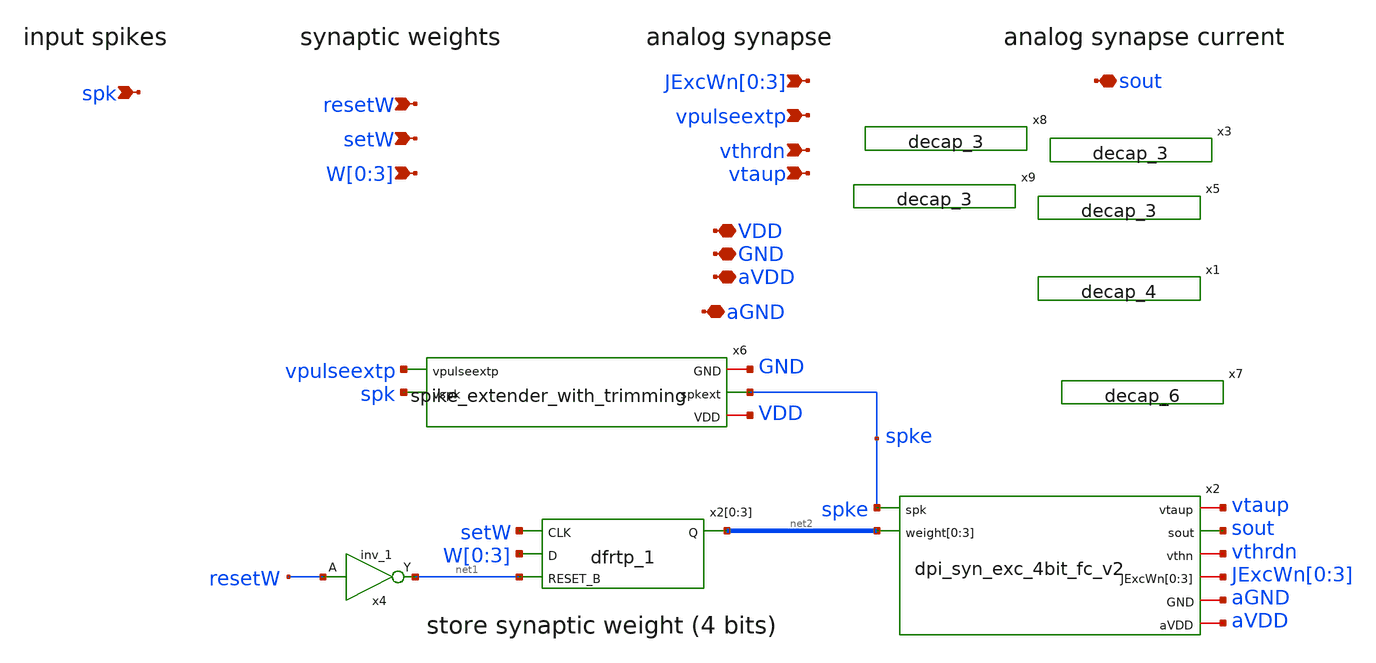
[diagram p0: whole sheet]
** sch_path: design/xschem/synapse_4bit_memory_v1_norail.sch
**.subckt synapse_4bit_memory_v1_norail GND VDD vpulseextp spk setW resetW sout vthrdn vtaup aVDD
*+ JExcWn[0],JExcWn[1],JExcWn[2],JExcWn[3] W[0],W[1],W[2],W[3] aGND
*.iopin GND
*.iopin VDD
*.ipin vpulseextp
*.ipin spk
*.ipin setW
*.ipin resetW
*.iopin sout
*.ipin vthrdn
*.ipin vtaup
*.iopin aVDD
*.ipin JExcWn[0],JExcWn[1],JExcWn[2],JExcWn[3]
*.ipin W[0],W[1],W[2],W[3]
*.iopin aGND
x2[0] setW W[0] net1 GND GND VDD VDD net2[3] sky130_fd_sc_hd__dfrtp_1
x2[1] setW W[1] net1 GND GND VDD VDD net2[2] sky130_fd_sc_hd__dfrtp_1
x2[2] setW W[2] net1 GND GND VDD VDD net2[1] sky130_fd_sc_hd__dfrtp_1
x2[3] setW W[3] net1 GND GND VDD VDD net2[0] sky130_fd_sc_hd__dfrtp_1
x4 resetW GND GND VDD VDD net1 sky130_fd_sc_hd__inv_1
x2 vtaup sout vthrdn spke JExcWn[0] JExcWn[1] JExcWn[2] JExcWn[3] aGND aVDD net2[3] net2[2] net2[1]
+ net2[0] dpi_syn_exc_4bit_fc_v2
x6 vpulseextp spk GND spke VDD spike_extender_with_trimming
x1 GND GND VDD VDD sky130_fd_sc_hd__decap_4
x3 GND GND VDD VDD sky130_fd_sc_hd__decap_3
x5 GND GND VDD VDD sky130_fd_sc_hd__decap_3
x7 GND GND VDD VDD sky130_fd_sc_hd__decap_6
x8 GND GND VDD VDD sky130_fd_sc_hd__decap_3
x9 GND GND VDD VDD sky130_fd_sc_hd__decap_3
**.ends

* expanding   symbol:  dpi_syn_exc_4bit_fc_v2.sym # of pins=8
** sym_path: design/xschem/dpi_syn_exc_4bit_fc_v2.sym
** sch_path: design/xschem/dpi_syn_exc_4bit_fc_v2.sch
.subckt dpi_syn_exc_4bit_fc_v2 vtaup sout vthn spk JExcWn[0] JExcWn[1] JExcWn[2] JExcWn[3] GND aVDD
+ weight[0] weight[1] weight[2] weight[3]
*.iopin GND
*.iopin aVDD
*.iopin vtaup
*.ipin spk
*.opin sout
*.iopin vthn
*.ipin weight[0],weight[1],weight[2],weight[3]
*.iopin JExcWn[0],JExcWn[1],JExcWn[2],JExcWn[3]
XM2 net3 spk net1 GND sky130_fd_pr__nfet_01v8 L=0.25 W=1.0 nf=1 ad='int((nf+1)/2) * W/nf * 0.29' as='int((nf+2)/2) * W/nf * 0.29'
+ pd='2*int((nf+1)/2) * (W/nf + 0.29)' ps='2*int((nf+2)/2) * (W/nf + 0.29)' nrd='0.29 / W' nrs='0.29 / W'
+ sa=0 sb=0 sd=0 mult=1 m=1
XC1 vsin aVDD sky130_fd_pr__cap_mim_m3_1 W=5 L=5 MF=1 m=1
XM5 vsin vtaup aVDD aVDD sky130_fd_pr__pfet_01v8 L=0.2 W=1.2 nf=1 ad='int((nf+1)/2) * W/nf * 0.29' as='int((nf+2)/2) * W/nf * 0.29'
+ pd='2*int((nf+1)/2) * (W/nf + 0.29)' ps='2*int((nf+2)/2) * (W/nf + 0.29)' nrd='0.29 / W' nrs='0.29 / W'
+ sa=0 sb=0 sd=0 mult=1 m=1
XM6 sout vsin aVDD aVDD sky130_fd_pr__pfet_01v8 L=0.2 W=1.2 nf=1 ad='int((nf+1)/2) * W/nf * 0.29' as='int((nf+2)/2) * W/nf * 0.29'
+ pd='2*int((nf+1)/2) * (W/nf + 0.29)' ps='2*int((nf+2)/2) * (W/nf + 0.29)' nrd='0.29 / W' nrs='0.29 / W'
+ sa=0 sb=0 sd=0 mult=1 m=1
XM1 net1 JExcWn[0] net2 GND sky130_fd_pr__nfet_01v8 L=1.0 W=1.0 nf=1 ad='int((nf+1)/2) * W/nf * 0.29'
+ as='int((nf+2)/2) * W/nf * 0.29' pd='2*int((nf+1)/2) * (W/nf + 0.29)' ps='2*int((nf+2)/2) * (W/nf + 0.29)'
+ nrd='0.29 / W' nrs='0.29 / W' sa=0 sb=0 sd=0 mult=1 m=1
XM4 vsin vsin net3 GND sky130_fd_pr__nfet_01v8 L=0.25 W=1.0 nf=1 ad='int((nf+1)/2) * W/nf * 0.29' as='int((nf+2)/2) * W/nf * 0.29'
+ pd='2*int((nf+1)/2) * (W/nf + 0.29)' ps='2*int((nf+2)/2) * (W/nf + 0.29)' nrd='0.29 / W' nrs='0.29 / W'
+ sa=0 sb=0 sd=0 mult=1 m=1
XM3 aVDD vthn net3 GND sky130_fd_pr__nfet_01v8 L=0.25 W=1.0 nf=1 ad='int((nf+1)/2) * W/nf * 0.29' as='int((nf+2)/2) * W/nf * 0.29'
+ pd='2*int((nf+1)/2) * (W/nf + 0.29)' ps='2*int((nf+2)/2) * (W/nf + 0.29)' nrd='0.29 / W' nrs='0.29 / W'
+ sa=0 sb=0 sd=0 mult=1 m=1
XM7 net1 JExcWn[1] net4 GND sky130_fd_pr__nfet_01v8 L=2.0 W=1.0 nf=1 ad='int((nf+1)/2) * W/nf * 0.29'
+ as='int((nf+2)/2) * W/nf * 0.29' pd='2*int((nf+1)/2) * (W/nf + 0.29)' ps='2*int((nf+2)/2) * (W/nf + 0.29)'
+ nrd='0.29 / W' nrs='0.29 / W' sa=0 sb=0 sd=0 mult=1 m=1
XM8 net1 JExcWn[2] net5 GND sky130_fd_pr__nfet_01v8 L=4.0 W=1.0 nf=1 ad='int((nf+1)/2) * W/nf * 0.29'
+ as='int((nf+2)/2) * W/nf * 0.29' pd='2*int((nf+1)/2) * (W/nf + 0.29)' ps='2*int((nf+2)/2) * (W/nf + 0.29)'
+ nrd='0.29 / W' nrs='0.29 / W' sa=0 sb=0 sd=0 mult=1 m=1
XM9 net1 JExcWn[3] net6 GND sky130_fd_pr__nfet_01v8 L=8.0 W=1.0 nf=1 ad='int((nf+1)/2) * W/nf * 0.29'
+ as='int((nf+2)/2) * W/nf * 0.29' pd='2*int((nf+1)/2) * (W/nf + 0.29)' ps='2*int((nf+2)/2) * (W/nf + 0.29)'
+ nrd='0.29 / W' nrs='0.29 / W' sa=0 sb=0 sd=0 mult=1 m=1
XM10 net2 weight[0] GND GND sky130_fd_pr__nfet_01v8 L=0.25 W=1.0 nf=1 ad='int((nf+1)/2) * W/nf * 0.29'
+ as='int((nf+2)/2) * W/nf * 0.29' pd='2*int((nf+1)/2) * (W/nf + 0.29)' ps='2*int((nf+2)/2) * (W/nf + 0.29)'
+ nrd='0.29 / W' nrs='0.29 / W' sa=0 sb=0 sd=0 mult=1 m=1
XM11 net4 weight[1] GND GND sky130_fd_pr__nfet_01v8 L=0.25 W=1.0 nf=1 ad='int((nf+1)/2) * W/nf * 0.29'
+ as='int((nf+2)/2) * W/nf * 0.29' pd='2*int((nf+1)/2) * (W/nf + 0.29)' ps='2*int((nf+2)/2) * (W/nf + 0.29)'
+ nrd='0.29 / W' nrs='0.29 / W' sa=0 sb=0 sd=0 mult=1 m=1
XM12 net5 weight[2] GND GND sky130_fd_pr__nfet_01v8 L=0.25 W=1.0 nf=1 ad='int((nf+1)/2) * W/nf * 0.29'
+ as='int((nf+2)/2) * W/nf * 0.29' pd='2*int((nf+1)/2) * (W/nf + 0.29)' ps='2*int((nf+2)/2) * (W/nf + 0.29)'
+ nrd='0.29 / W' nrs='0.29 / W' sa=0 sb=0 sd=0 mult=1 m=1
XM13 net6 weight[3] GND GND sky130_fd_pr__nfet_01v8 L=0.25 W=1.0 nf=1 ad='int((nf+1)/2) * W/nf * 0.29'
+ as='int((nf+2)/2) * W/nf * 0.29' pd='2*int((nf+1)/2) * (W/nf + 0.29)' ps='2*int((nf+2)/2) * (W/nf + 0.29)'
+ nrd='0.29 / W' nrs='0.29 / W' sa=0 sb=0 sd=0 mult=1 m=1
.ends


* expanding   symbol:  spike_extender_with_trimming.sym # of pins=5
** sym_path: design/xschem/spike_extender_with_trimming.sym
** sch_path: design/xschem/spike_extender_with_trimming.sch
.subckt spike_extender_with_trimming vpulseextp vspk GND spkext VDD
*.iopin GND
*.iopin VDD
*.ipin vspk
*.opin spkext
*.ipin vpulseextp
x1 vpulseextp vpulseshort GND spkext VDD spike_extender
x3 vspk GND GND VDD VDD net1 sky130_fd_sc_hd__clkdlybuf4s50_1
x2 net1 vspk GND GND VDD VDD vpulseshort sky130_fd_sc_hd__nor2b_1
.ends


* expanding   symbol:  spike_extender.sym # of pins=5
** sym_path: design/xschem/spike_extender.sym
** sch_path: design/xschem/spike_extender.sch
.subckt spike_extender vpulseextp spk GND spkext VDD
*.iopin GND
*.iopin VDD
*.ipin spk
*.opin spkext
*.ipin vpulseextp
XM1 net1 spk GND GND sky130_fd_pr__nfet_01v8 L=0.15 W=0.65 nf=1 ad='int((nf+1)/2) * W/nf * 0.29' as='int((nf+2)/2) * W/nf * 0.29'
+ pd='2*int((nf+1)/2) * (W/nf + 0.29)' ps='2*int((nf+2)/2) * (W/nf + 0.29)' nrd='0.29 / W' nrs='0.29 / W'
+ sa=0 sb=0 sd=0 mult=1 m=1
XM6 net1 vpulseextp VDD VDD sky130_fd_pr__pfet_01v8 L=2 W=1 nf=1 ad='int((nf+1)/2) * W/nf * 0.29' as='int((nf+2)/2) * W/nf * 0.29'
+ pd='2*int((nf+1)/2) * (W/nf + 0.29)' ps='2*int((nf+2)/2) * (W/nf + 0.29)' nrd='0.29 / W' nrs='0.29 / W'
+ sa=0 sb=0 sd=0 mult=1 m=1
XM5 net3 net2 GND GND sky130_fd_pr__nfet_01v8 L=0.15 W=0.65 nf=1 ad='int((nf+1)/2) * W/nf * 0.29' as='int((nf+2)/2) * W/nf * 0.29'
+ pd='2*int((nf+1)/2) * (W/nf + 0.29)' ps='2*int((nf+2)/2) * (W/nf + 0.29)' nrd='0.29 / W' nrs='0.29 / W'
+ sa=0 sb=0 sd=0 mult=1 m=1
XM8 spkext net3 GND GND sky130_fd_pr__nfet_01v8 L=0.15 W=0.65 nf=1 ad='int((nf+1)/2) * W/nf * 0.29' as='int((nf+2)/2) * W/nf * 0.29'
+ pd='2*int((nf+1)/2) * (W/nf + 0.29)' ps='2*int((nf+2)/2) * (W/nf + 0.29)' nrd='0.29 / W' nrs='0.29 / W'
+ sa=0 sb=0 sd=0 mult=1 m=1
XM4 net3 net2 VDD VDD sky130_fd_pr__pfet_01v8 L=0.15 W=1.0 nf=1 ad='int((nf+1)/2) * W/nf * 0.29' as='int((nf+2)/2) * W/nf * 0.29'
+ pd='2*int((nf+1)/2) * (W/nf + 0.29)' ps='2*int((nf+2)/2) * (W/nf + 0.29)' nrd='0.29 / W' nrs='0.29 / W'
+ sa=0 sb=0 sd=0 mult=1 m=1
XM7 spkext net3 VDD VDD sky130_fd_pr__pfet_01v8 L=0.15 W=1.0 nf=1 ad='int((nf+1)/2) * W/nf * 0.29' as='int((nf+2)/2) * W/nf * 0.29'
+ pd='2*int((nf+1)/2) * (W/nf + 0.29)' ps='2*int((nf+2)/2) * (W/nf + 0.29)' nrd='0.29 / W' nrs='0.29 / W'
+ sa=0 sb=0 sd=0 mult=1 m=1
XM2 net2 net1 GND GND sky130_fd_pr__nfet_01v8 L=0.15 W=0.65 nf=1 ad='int((nf+1)/2) * W/nf * 0.29' as='int((nf+2)/2) * W/nf * 0.29'
+ pd='2*int((nf+1)/2) * (W/nf + 0.29)' ps='2*int((nf+2)/2) * (W/nf + 0.29)' nrd='0.29 / W' nrs='0.29 / W'
+ sa=0 sb=0 sd=0 mult=1 m=1
XM3 net2 net1 VDD VDD sky130_fd_pr__pfet_01v8 L=0.15 W=1.0 nf=1 ad='int((nf+1)/2) * W/nf * 0.29' as='int((nf+2)/2) * W/nf * 0.29'
+ pd='2*int((nf+1)/2) * (W/nf + 0.29)' ps='2*int((nf+2)/2) * (W/nf + 0.29)' nrd='0.29 / W' nrs='0.29 / W'
+ sa=0 sb=0 sd=0 mult=1 m=1
XM9 GND net1 GND GND sky130_fd_pr__nfet_01v8 L=1 W=0.65 nf=1 ad='int((nf+1)/2) * W/nf * 0.29' as='int((nf+2)/2) * W/nf * 0.29'
+ pd='2*int((nf+1)/2) * (W/nf + 0.29)' ps='2*int((nf+2)/2) * (W/nf + 0.29)' nrd='0.29 / W' nrs='0.29 / W'
+ sa=0 sb=0 sd=0 mult=1 m=1
.ends

.end
